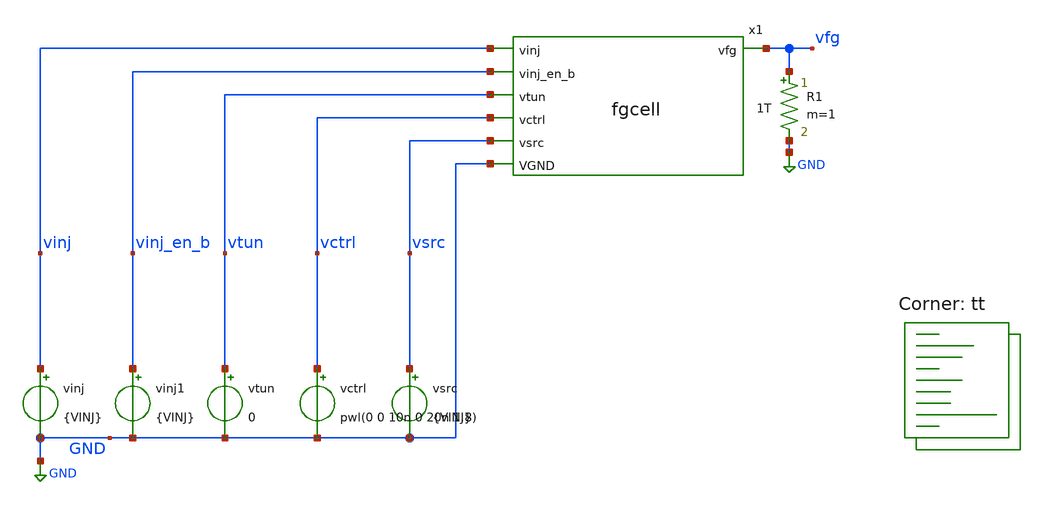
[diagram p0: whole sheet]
** sch_path: xschem/test-fgcell.sch
**.subckt test-fgcell
x1 vinj vinj_en_b vfg vtun vctrl vsrc GND fgcell
vinj1 vinj_en_b GND {VINJ}
vctrl vctrl GND pwl(0 0 10n 0 20n 1.8)
vsrc vsrc GND {VINJ}
vtun vtun GND 0
vinj vinj GND {VINJ}
R1 vfg GND 1T m=1
**** begin user architecture code
.lib $::SKYWATER_MODELS/sky130.lib.spice tt



.param VINJ=6
.param VDD=1.8
.param VSS=0
.option savecurrents
.ic v(vfg)=0
.control
  save all
  op
  remzerovec
  write test-fgcell.raw
  set appendwrite
  tran 10p 30n uic
  remzerovec
  write test-fgcell.raw
.endc



**** end user architecture code
**.ends

* expanding   symbol:  fgcell.sym # of pins=7
** sym_path: xschem/fgcell.sym
** sch_path: xschem/fgcell.sch
.subckt fgcell vinj vinj_en_b vfg vtun vctrl vsrc VGND
*.ipin vctrl
*.ipin vtun
*.ipin vinj
*.ipin vinj_en_b
*.ipin vsrc
*.opin vfg
*.ipin VGND
XC1 vfg vtun vtun sky130_fd_pr__cap_var_hvt W=0.5 L=0.5 VM=1 m=1
XM1 vsrc vfg net1 vinj sky130_fd_pr__pfet_g5v0d10v5 L=0.5 W=1 nf=1 ad='int((nf+1)/2) * W/nf * 0.29' as='int((nf+2)/2) * W/nf * 0.29'
+ pd='2*int((nf+1)/2) * (W/nf + 0.29)' ps='2*int((nf+2)/2) * (W/nf + 0.29)' nrd='0.29 / W' nrs='0.29 / W'
+ sa=0 sb=0 sd=0 mult=1 m=1
XM2 net1 vinj_en_b vinj vinj sky130_fd_pr__pfet_g5v0d10v5 L=0.5 W=1 nf=1 ad='int((nf+1)/2) * W/nf * 0.29'
+ as='int((nf+2)/2) * W/nf * 0.29' pd='2*int((nf+1)/2) * (W/nf + 0.29)' ps='2*int((nf+2)/2) * (W/nf + 0.29)'
+ nrd='0.29 / W' nrs='0.29 / W' sa=0 sb=0 sd=0 mult=1 m=1
XM3 vctrl vfg vctrl vctrl sky130_fd_pr__pfet_g5v0d10v5 L=0.5 W=1 nf=1 ad='int((nf+1)/2) * W/nf * 0.29'
+ as='int((nf+2)/2) * W/nf * 0.29' pd='2*int((nf+1)/2) * (W/nf + 0.29)' ps='2*int((nf+2)/2) * (W/nf + 0.29)'
+ nrd='0.29 / W' nrs='0.29 / W' sa=0 sb=0 sd=0 mult=1 m=1
.ends

.GLOBAL GND
.end
